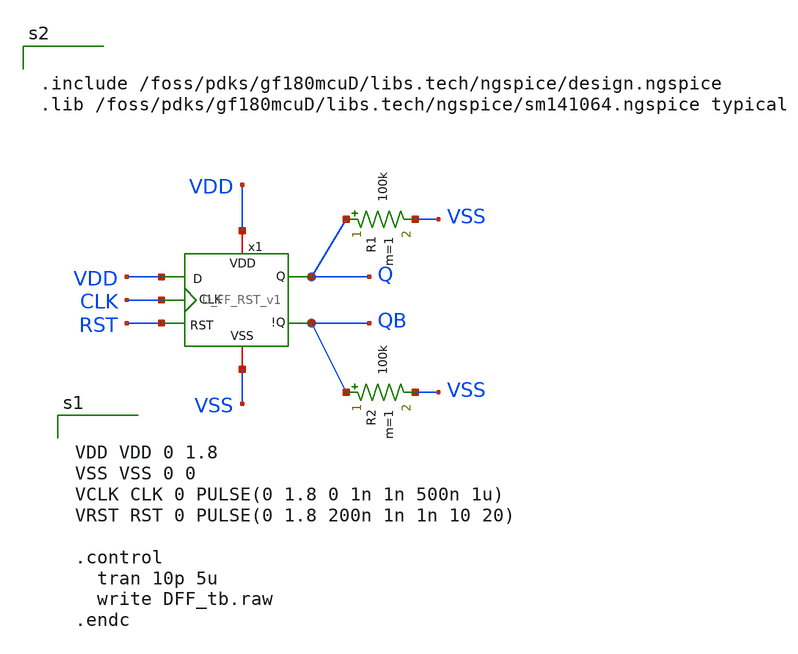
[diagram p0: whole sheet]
** sch_path: team_src/xschem/D_FF_RST_v1_tb.sch
**.subckt D_FF_RST_v1_tb
x1 RST VDD VDD Q CLK QB VSS D_FF_RST_v1
R1 Q VSS 100k m=1
R2 QB VSS 100k m=1
**** begin user architecture code


VDD VDD 0 1.8
VSS VSS 0 0
VCLK CLK 0 PULSE(0 1.8 0 1n 1n 500n 1u)
VRST RST 0 PULSE(0 1.8 200n 1n 1n 10 20)

.control
  tran 10p 5u
  write DFF_tb.raw
.endc




.include /foss/pdks/gf180mcuD/libs.tech/ngspice/design.ngspice
.lib /foss/pdks/gf180mcuD/libs.tech/ngspice/sm141064.ngspice typical


**** end user architecture code
**.ends

* expanding   symbol:  D_FF_RST_v1.sym # of pins=7
** sym_path: team_src/xschem/D_FF_RST_v1.sym
** sch_path: team_src/xschem/D_FF_RST_v1.sch
.subckt D_FF_RST_v1 RST VDD D Q CLK !Q VSS
*.ipin CLK
*.ipin D
*.iopin VDD
*.opin Q
*.opin !Q
*.iopin VSS
*.ipin RST
*.iopin VDD
*.iopin VDD
*.iopin VSS
*.iopin VSS
*.iopin VDD
*.iopin VDD
*.iopin VDD
*.iopin VDD
*.iopin VSS
*.iopin VSS
*.iopin VSS
*.iopin VSS
x1 VDD Q net4 !Q VSS NAND_v1
x3 VDD net6 D net2 VSS NAND_v1
x4 VDD net5 net1 net2 VSS NAND_v1
x5 VDD D net1 VSS NOT_v1
x6 VDD net3 net2 VSS NOT_v1
x7 VDD CLK CLKB VSS NOT_v1
x8 VDD net3 CLK CLKB_DLY VSS NAND_v1
x2 RST VDD !Q Q net5 VSS NAND3_v1
x9 VDD net6 net7 VSS NOT_v1
x10 VDD net4 net7 RST VSS NAND_v1
x11 VDD CLKB net8 VSS NOT_v1
x12 VDD net12 CLKB_DLY VSS NOT_v1
x13 VDD net8 net9 VSS NOT_v1
x14 VDD net9 net10 VSS NOT_v1
x15 VDD net10 net11 VSS NOT_v1
x16 VDD net11 net12 VSS NOT_v1
.ends


* expanding   symbol:  NAND_v1.sym # of pins=5
** sym_path: team_src/xschem/NAND_v1.sym
** sch_path: team_src/xschem/NAND_v1.sch
.subckt NAND_v1 VDD Y A B VSS
*.iopin VSS
*.iopin VDD
*.ipin A
*.opin Y
*.ipin B
XM1 net1 B VSS VSS nfet_03v3 L=0.28u W=1u nf=1 ad='int((nf+1)/2) * W/nf * 0.18u' as='int((nf+2)/2) * W/nf * 0.18u'
+ pd='2*int((nf+1)/2) * (W/nf + 0.18u)' ps='2*int((nf+2)/2) * (W/nf + 0.18u)' nrd='0.18u / W' nrs='0.18u / W'
+ sa=0 sb=0 sd=0 m=1
XM2 Y A net1 VSS nfet_03v3 L=0.28u W=1u nf=1 ad='int((nf+1)/2) * W/nf * 0.18u' as='int((nf+2)/2) * W/nf * 0.18u'
+ pd='2*int((nf+1)/2) * (W/nf + 0.18u)' ps='2*int((nf+2)/2) * (W/nf + 0.18u)' nrd='0.18u / W' nrs='0.18u / W'
+ sa=0 sb=0 sd=0 m=1
XM3 Y B VDD VDD pfet_03v3 L=0.28u W=1u nf=1 ad='int((nf+1)/2) * W/nf * 0.18u' as='int((nf+2)/2) * W/nf * 0.18u'
+ pd='2*int((nf+1)/2) * (W/nf + 0.18u)' ps='2*int((nf+2)/2) * (W/nf + 0.18u)' nrd='0.18u / W' nrs='0.18u / W'
+ sa=0 sb=0 sd=0 m=1
XM4 Y A VDD VDD pfet_03v3 L=0.28u W=1u nf=1 ad='int((nf+1)/2) * W/nf * 0.18u' as='int((nf+2)/2) * W/nf * 0.18u'
+ pd='2*int((nf+1)/2) * (W/nf + 0.18u)' ps='2*int((nf+2)/2) * (W/nf + 0.18u)' nrd='0.18u / W' nrs='0.18u / W'
+ sa=0 sb=0 sd=0 m=1
.ends


* expanding   symbol:  NOT_v1.sym # of pins=4
** sym_path: team_src/xschem/NOT_v1.sym
** sch_path: team_src/xschem/NOT_v1.sch
.subckt NOT_v1 VDD A Y VSS
*.iopin VSS
*.iopin VDD
*.ipin A
*.opin Y
XM2 Y A VSS VSS nfet_03v3 L=0.28u W=1u nf=1 ad='int((nf+1)/2) * W/nf * 0.18u' as='int((nf+2)/2) * W/nf * 0.18u'
+ pd='2*int((nf+1)/2) * (W/nf + 0.18u)' ps='2*int((nf+2)/2) * (W/nf + 0.18u)' nrd='0.18u / W' nrs='0.18u / W'
+ sa=0 sb=0 sd=0 m=1
XM4 Y A VDD VDD pfet_03v3 L=0.28u W=1u nf=1 ad='int((nf+1)/2) * W/nf * 0.18u' as='int((nf+2)/2) * W/nf * 0.18u'
+ pd='2*int((nf+1)/2) * (W/nf + 0.18u)' ps='2*int((nf+2)/2) * (W/nf + 0.18u)' nrd='0.18u / W' nrs='0.18u / W'
+ sa=0 sb=0 sd=0 m=1
.ends


* expanding   symbol:  NAND3_v1.sym # of pins=6
** sym_path: team_src/xschem/NAND3_v1.sym
** sch_path: team_src/xschem/NAND3_v1.sch
.subckt NAND3_v1 C VDD Y A B VSS
*.iopin VSS
*.iopin VDD
*.ipin A
*.opin Y
*.ipin B
*.ipin C
XM1 net1 B net2 VSS nfet_03v3 L=0.28u W=3u nf=1 ad='int((nf+1)/2) * W/nf * 0.18u' as='int((nf+2)/2) * W/nf * 0.18u'
+ pd='2*int((nf+1)/2) * (W/nf + 0.18u)' ps='2*int((nf+2)/2) * (W/nf + 0.18u)' nrd='0.18u / W' nrs='0.18u / W'
+ sa=0 sb=0 sd=0 m=1
XM2 Y A net1 VSS nfet_03v3 L=0.28u W=3u nf=1 ad='int((nf+1)/2) * W/nf * 0.18u' as='int((nf+2)/2) * W/nf * 0.18u'
+ pd='2*int((nf+1)/2) * (W/nf + 0.18u)' ps='2*int((nf+2)/2) * (W/nf + 0.18u)' nrd='0.18u / W' nrs='0.18u / W'
+ sa=0 sb=0 sd=0 m=1
XM3 Y B VDD VDD pfet_03v3 L=0.28u W=1u nf=1 ad='int((nf+1)/2) * W/nf * 0.18u' as='int((nf+2)/2) * W/nf * 0.18u'
+ pd='2*int((nf+1)/2) * (W/nf + 0.18u)' ps='2*int((nf+2)/2) * (W/nf + 0.18u)' nrd='0.18u / W' nrs='0.18u / W'
+ sa=0 sb=0 sd=0 m=1
XM4 Y A VDD VDD pfet_03v3 L=0.28u W=1u nf=1 ad='int((nf+1)/2) * W/nf * 0.18u' as='int((nf+2)/2) * W/nf * 0.18u'
+ pd='2*int((nf+1)/2) * (W/nf + 0.18u)' ps='2*int((nf+2)/2) * (W/nf + 0.18u)' nrd='0.18u / W' nrs='0.18u / W'
+ sa=0 sb=0 sd=0 m=1
XM5 Y C VDD VDD pfet_03v3 L=0.28u W=1u nf=1 ad='int((nf+1)/2) * W/nf * 0.18u' as='int((nf+2)/2) * W/nf * 0.18u'
+ pd='2*int((nf+1)/2) * (W/nf + 0.18u)' ps='2*int((nf+2)/2) * (W/nf + 0.18u)' nrd='0.18u / W' nrs='0.18u / W'
+ sa=0 sb=0 sd=0 m=1
XM6 net2 C VSS VSS nfet_03v3 L=0.28u W=3u nf=1 ad='int((nf+1)/2) * W/nf * 0.18u' as='int((nf+2)/2) * W/nf * 0.18u'
+ pd='2*int((nf+1)/2) * (W/nf + 0.18u)' ps='2*int((nf+2)/2) * (W/nf + 0.18u)' nrd='0.18u / W' nrs='0.18u / W'
+ sa=0 sb=0 sd=0 m=1
.ends

.end
